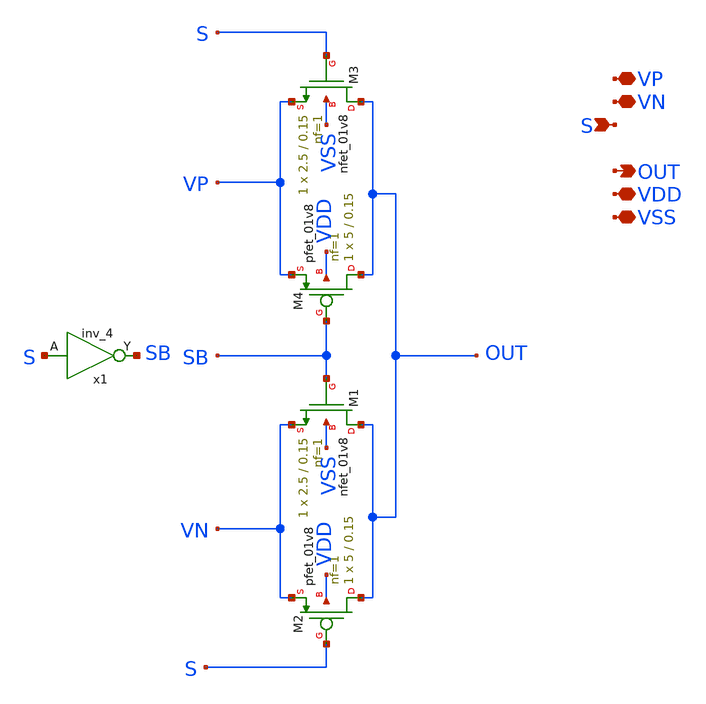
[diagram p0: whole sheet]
** sch_path: xschem/sar-adc/tgmux.sch
**.subckt tgmux VP VN S OUT VDD VSS
*.iopin VP
*.iopin VN
*.ipin S
*.opin OUT
*.iopin VDD
*.iopin VSS
XM1 OUT SB VN VSS sky130_fd_pr__nfet_01v8 L=0.15 W=2.5 nf=1 ad='int((1 + 1)/2) * 2.5 / 1 * 0.29' as='int((1 + 2)/2) * 2.5 / 1 * 0.29'
+ pd='2*int((1 + 1)/2) * (2.5 / 1 + 0.29)' ps='2*int((1 + 2)/2) * (2.5 / 1 + 0.29)' nrd='0.29 / 2.5 ' nrs='0.29 / 2.5 '
+ sa=0 sb=0 sd=0 mult=1 m=1
XM2 OUT S VN VDD sky130_fd_pr__pfet_01v8 L=0.15 W=5 nf=1 ad='int((1 + 1)/2) * 5 / 1 * 0.29' as='int((1 + 2)/2) * 5 / 1 * 0.29'
+ pd='2*int((1 + 1)/2) * (5 / 1 + 0.29)' ps='2*int((1 + 2)/2) * (5 / 1 + 0.29)' nrd='0.29 / 5 ' nrs='0.29 / 5 '
+ sa=0 sb=0 sd=0 mult=1 m=1
XM3 OUT S VP VSS sky130_fd_pr__nfet_01v8 L=0.15 W=2.5 nf=1 ad='int((1 + 1)/2) * 2.5 / 1 * 0.29' as='int((1 + 2)/2) * 2.5 / 1 * 0.29'
+ pd='2*int((1 + 1)/2) * (2.5 / 1 + 0.29)' ps='2*int((1 + 2)/2) * (2.5 / 1 + 0.29)' nrd='0.29 / 2.5 ' nrs='0.29 / 2.5 '
+ sa=0 sb=0 sd=0 mult=1 m=1
XM4 OUT SB VP VDD sky130_fd_pr__pfet_01v8 L=0.15 W=5 nf=1 ad='int((1 + 1)/2) * 5 / 1 * 0.29' as='int((1 + 2)/2) * 5 / 1 * 0.29'
+ pd='2*int((1 + 1)/2) * (5 / 1 + 0.29)' ps='2*int((1 + 2)/2) * (5 / 1 + 0.29)' nrd='0.29 / 5 ' nrs='0.29 / 5 '
+ sa=0 sb=0 sd=0 mult=1 m=1
x1 S VSS VSS VDD VDD SB sky130_fd_sc_hd__inv_4
**.ends
.end
